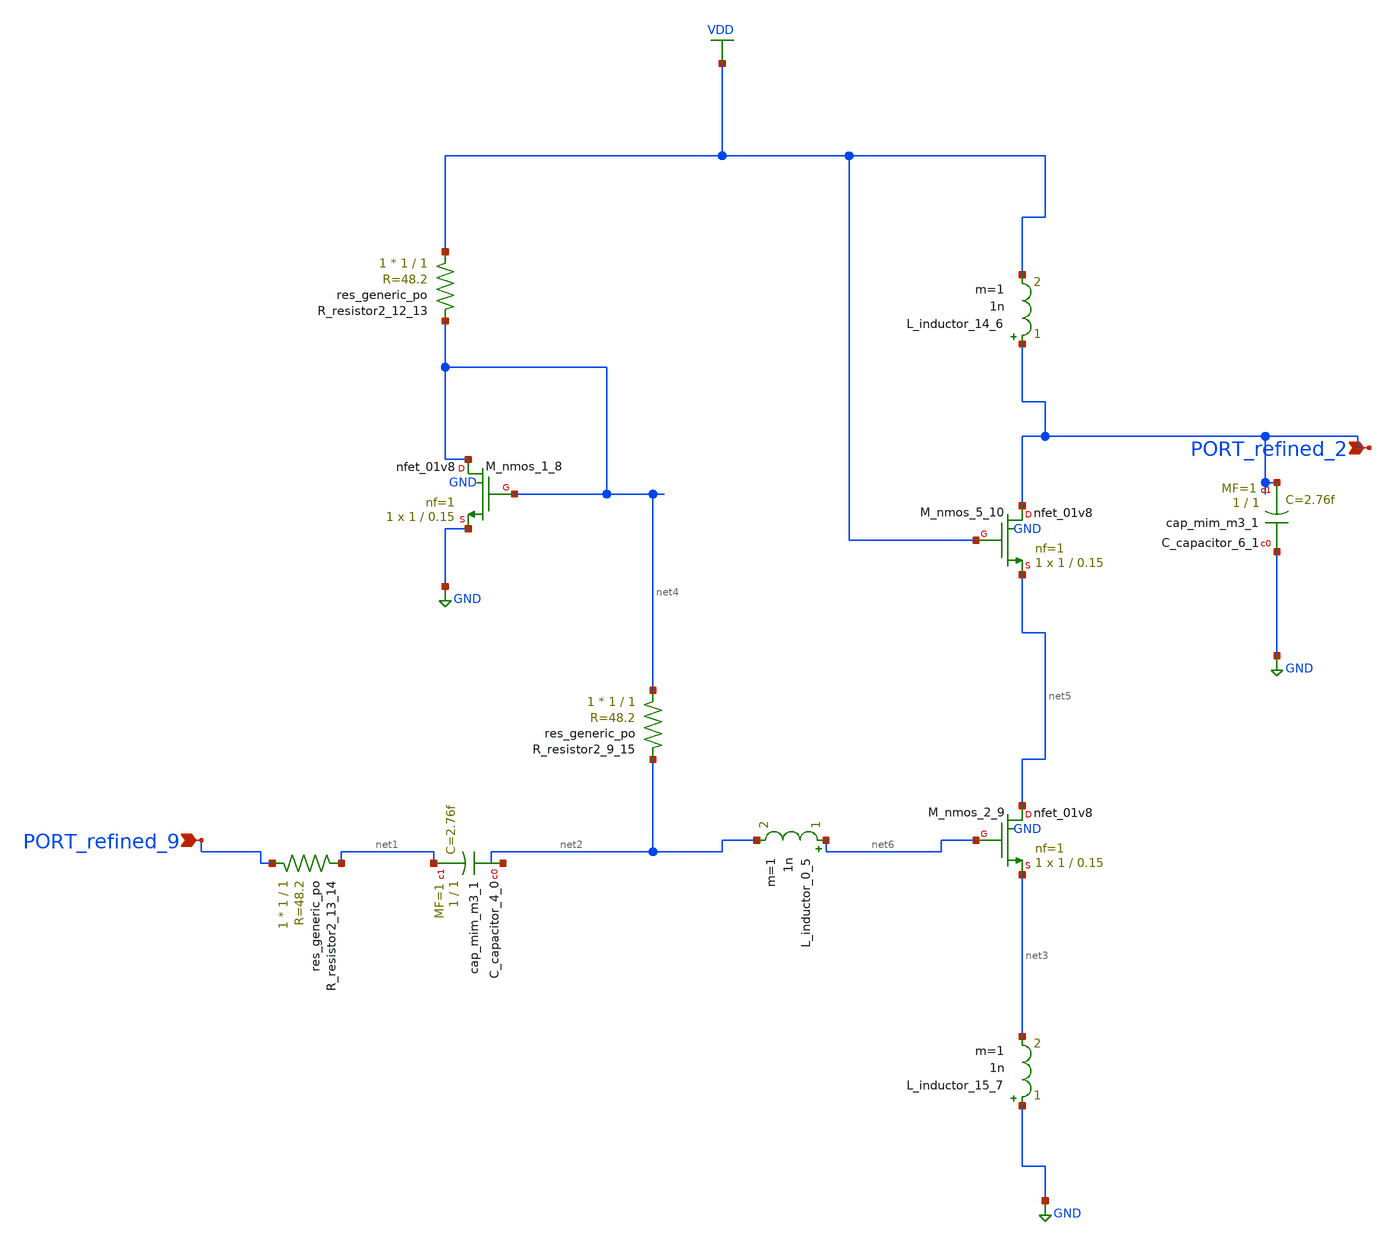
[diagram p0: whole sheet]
** sch_path: schematics/SchemGen/p03_fig3_cascode_lna.sch
**.subckt p03_fig3_cascode_lna PORT_refined_9 PORT_refined_2
*.ipin PORT_refined_9
*.ipin PORT_refined_2
XC_capacitor_4_0 net2 net1 sky130_fd_pr__cap_mim_m3_1 W=1 L=1 MF=1 m=1
XC_capacitor_6_1 GND PORT_refined_2 sky130_fd_pr__cap_mim_m3_1 W=1 L=1 MF=1 m=1
L_inductor_0_5 net6 net2 1n m=1
L_inductor_14_6 PORT_refined_2 VDD 1n m=1
L_inductor_15_7 GND net3 1n m=1
XM_nmos_1_8 net4 net4 GND GND sky130_fd_pr__nfet_01v8 L=0.15 W=1 nf=1 ad='int((1 + 1)/2) * 1 / 1 * 0.29'
+ as='int((1 + 2)/2) * 1 / 1 * 0.29' pd='2*int((1 + 1)/2) * (1 / 1 + 0.29)' ps='2*int((1 + 2)/2) * (1 / 1 + 0.29)'
+ nrd='0.29 / 1 ' nrs='0.29 / 1 ' sa=0 sb=0 sd=0 mult=1 m=1
XM_nmos_2_9 net5 net6 net3 GND sky130_fd_pr__nfet_01v8 L=0.15 W=1 nf=1 ad='int((1 + 1)/2) * 1 / 1 * 0.29'
+ as='int((1 + 2)/2) * 1 / 1 * 0.29' pd='2*int((1 + 1)/2) * (1 / 1 + 0.29)' ps='2*int((1 + 2)/2) * (1 / 1 + 0.29)'
+ nrd='0.29 / 1 ' nrs='0.29 / 1 ' sa=0 sb=0 sd=0 mult=1 m=1
XM_nmos_5_10 PORT_refined_2 VDD net5 GND sky130_fd_pr__nfet_01v8 L=0.15 W=1 nf=1 ad='int((1 + 1)/2) * 1 / 1 * 0.29'
+ as='int((1 + 2)/2) * 1 / 1 * 0.29' pd='2*int((1 + 1)/2) * (1 / 1 + 0.29)' ps='2*int((1 + 2)/2) * (1 / 1 + 0.29)'
+ nrd='0.29 / 1 ' nrs='0.29 / 1 ' sa=0 sb=0 sd=0 mult=1 m=1
XR_resistor2_12_13 VDD net4 sky130_fd_pr__res_generic_po W=1 L=1 m=1
XR_resistor2_13_14 PORT_refined_9 net1 sky130_fd_pr__res_generic_po W=1 L=1 m=1
XR_resistor2_9_15 net4 net2 sky130_fd_pr__res_generic_po W=1 L=1 m=1
**.ends
.GLOBAL GND
.GLOBAL VDD
.end
